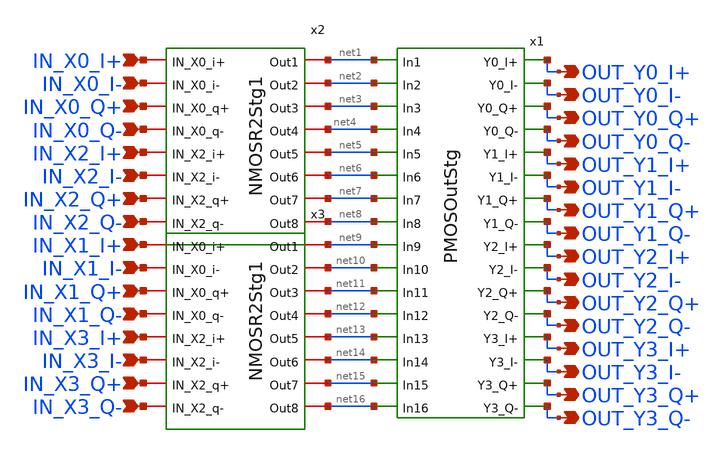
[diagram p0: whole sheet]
** sch_path: xschem/FinalProject/AnalogFFT.sch
**.subckt AnalogFFT IN_X0_I+ OUT_Y0_I+ IN_X0_I- OUT_Y0_I- IN_X0_Q+ OUT_Y0_Q+ IN_X0_Q- OUT_Y0_Q-
*+ IN_X2_I+ OUT_Y1_I+ IN_X2_I- OUT_Y1_I- IN_X2_Q+ OUT_Y1_Q+ IN_X2_Q- OUT_Y1_Q- IN_X1_I+ OUT_Y2_I+ IN_X1_I-
*+ OUT_Y2_I- IN_X1_Q+ OUT_Y2_Q+ IN_X1_Q- OUT_Y2_Q- IN_X3_I+ OUT_Y3_I+ IN_X3_I- OUT_Y3_I- IN_X3_Q+ OUT_Y3_Q+
*+ IN_X3_Q- OUT_Y3_Q-
*.ipin IN_X0_I+
*.opin OUT_Y0_I+
*.ipin IN_X0_I-
*.opin OUT_Y0_I-
*.ipin IN_X0_Q+
*.opin OUT_Y0_Q+
*.ipin IN_X0_Q-
*.opin OUT_Y0_Q-
*.ipin IN_X2_I+
*.opin OUT_Y1_I+
*.ipin IN_X2_I-
*.opin OUT_Y1_I-
*.ipin IN_X2_Q+
*.opin OUT_Y1_Q+
*.ipin IN_X2_Q-
*.opin OUT_Y1_Q-
*.ipin IN_X1_I+
*.opin OUT_Y2_I+
*.ipin IN_X1_I-
*.opin OUT_Y2_I-
*.ipin IN_X1_Q+
*.opin OUT_Y2_Q+
*.ipin IN_X1_Q-
*.opin OUT_Y2_Q-
*.ipin IN_X3_I+
*.opin OUT_Y3_I+
*.ipin IN_X3_I-
*.opin OUT_Y3_I-
*.ipin IN_X3_Q+
*.opin OUT_Y3_Q+
*.ipin IN_X3_Q-
*.opin OUT_Y3_Q-
x1 net1 OUT_Y0_I+ net2 OUT_Y0_I- net3 OUT_Y0_Q+ net4 OUT_Y0_Q- net5 OUT_Y1_I+ net6 OUT_Y1_I- net7
+ OUT_Y1_Q+ net8 OUT_Y1_Q- net9 OUT_Y2_I+ net10 OUT_Y2_I- net11 OUT_Y2_Q+ net12 OUT_Y2_Q- net13 OUT_Y3_I+ net14
+ OUT_Y3_I- net15 OUT_Y3_Q+ net16 OUT_Y3_Q- PMOSOutStg
x2 IN_X0_I+ net1 IN_X0_I- net2 IN_X0_Q+ net3 IN_X0_Q- net4 IN_X2_I+ net5 IN_X2_I- net6 IN_X2_Q+ net7
+ IN_X2_Q- net8 NMOSR2Stg1
x3 IN_X1_I+ net9 IN_X1_I- net10 IN_X1_Q+ net11 IN_X1_Q- net12 IN_X3_I+ net13 IN_X3_I- net14 IN_X3_Q+
+ net15 IN_X3_Q- net16 NMOSR2Stg1
**.ends
.end
